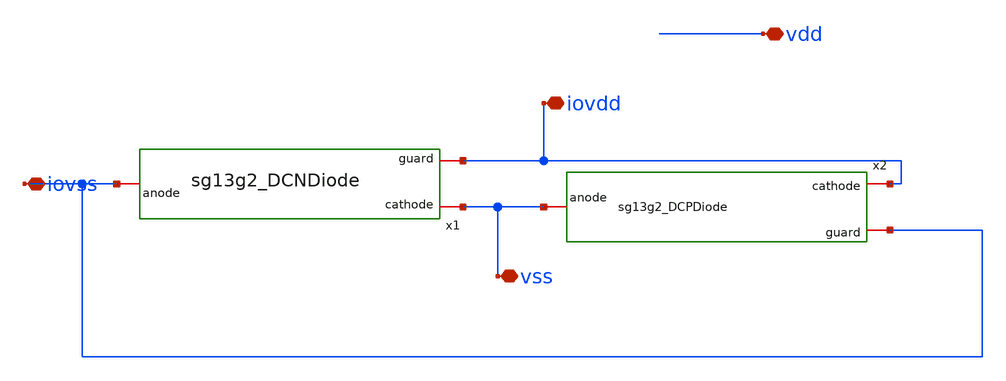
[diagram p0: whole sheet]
** sch_path: ihp-sg13g2/libs.ref/sg13g2_io/xschem/sg13g2_IOPadVSS.sch
**.subckt sg13g2_IOPadVSS iovss iovdd vss vdd
*.iopin iovss
*.iopin iovdd
*.iopin vss
*.iopin vdd
x1 vss iovss iovdd sg13g2_DCNDiode
x2 iovdd vss iovss sg13g2_DCPDiode
**.ends

* expanding   symbol:
*+  /home/prabhat.dubey/OPEN_Source_IHP_PDK/IHP-Open-PDK/ihp-sg13g2/libs.ref/sg13g2_io/xschem/sg13g2_DCNDiode.sym # of pins=3
** sym_path: ihp-sg13g2/libs.ref/sg13g2_io/xschem/sg13g2_DCNDiode.sym
** sch_path: ihp-sg13g2/libs.ref/sg13g2_io/xschem/sg13g2_DCNDiode.sch
.subckt sg13g2_DCNDiode cathode anode guard
*.iopin cathode
*.iopin anode
*.iopin guard
XD1 anode cathode dantenna l=1.26u w=27.78u
XD2 anode cathode dantenna l=1.26u w=27.78u
.ends


* expanding   symbol:
*+  /home/prabhat.dubey/OPEN_Source_IHP_PDK/IHP-Open-PDK/ihp-sg13g2/libs.ref/sg13g2_io/xschem/sg13g2_DCPDiode.sym # of pins=3
** sym_path: ihp-sg13g2/libs.ref/sg13g2_io/xschem/sg13g2_DCPDiode.sym
** sch_path: ihp-sg13g2/libs.ref/sg13g2_io/xschem/sg13g2_DCPDiode.sch
.subckt sg13g2_DCPDiode cathode anode guard
*.iopin cathode
*.iopin anode
*.iopin guard
XD1 anode cathode dpantenna l=1.26u w=27.78u
XD2 anode cathode dpantenna l=1.26u w=27.78u
.ends

.end
